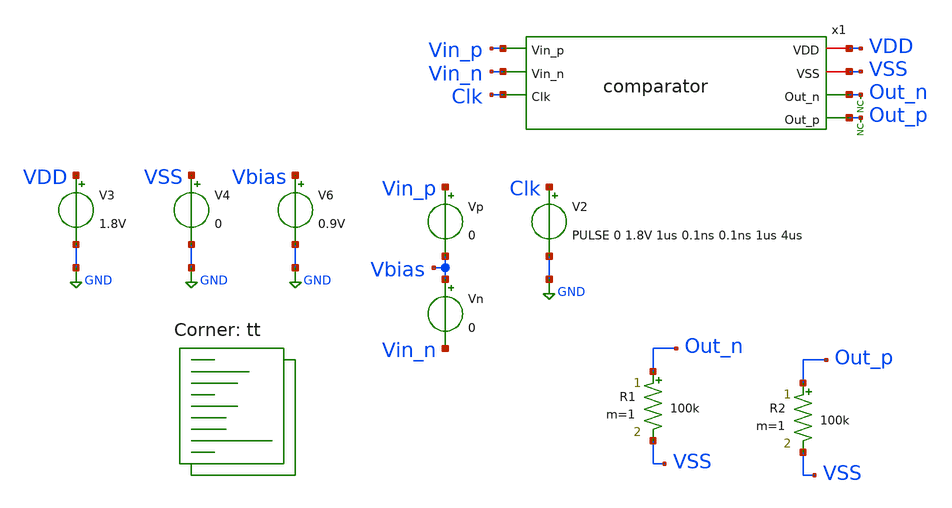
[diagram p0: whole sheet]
** sch_path: xschem/tests/comparator/comparator_stepped_test2.sch
**.subckt comparator_stepped_test2
V3 VDD GND 1.8V
V4 VSS GND 0
x1 VDD VSS Vin_p Out_n Vin_n Out_p Clk comparator
Vp Vin_p Vbias 0
V2 Clk GND PULSE 0 1.8V 1us 0.1ns 0.1ns 1us 4us
* noconn Out_p
* noconn Out_n
Vn Vbias Vin_n 0
V6 Vbias GND 0.9V
R1 Out_n VSS 100k m=1
R2 Out_p VSS 100k m=1
**** begin user architecture code
 *.lib $::SKYWATER_MODELS/sky130.lib.spice tt
.include $::SKYWATER_STDCELLS/sky130_fd_sc_hd.spice

.lib $::SKYWATER_MODELS/sky130.lib.spice tt



* ngspice commands


.control
save all
let vdiff = -0.1V
let vmax = 0.1V
let vdelta = 1.8e-2;
let runs = 0
let bad = 0
set sum_file = comparator_test_issues.txt
let bad_vdiffs = 0
set wr_vecnames

while vdiff le $&vmax
	alter vp vdiff
	alter vn vdiff
	tran 0.01u 3u
	*plot vin_p-vin_n out_p+4 out_n+4
	meas tran p_max MAX v(out_p) from=0u to=3u
	meas tran n_max MAX v(out_n) from=0u to=3u

	if $&vdiff > 0
		if $&p_max > 0.9
			if $&n_max < 0.9
				echo Good: $&vdiff
			else
				*compose bad_vdiffs values $&bad_vdiffs $&vdiff

				set fn = test_comparator_step_{$&vdiff}.txt
				echo Writing $fn
				wrdata $fn out_n out_p

				let bad = bad + 1

				echo Bad: $&vdiff
			end
		else
			*compose bad_vdiffs values $&bad_vdiffs $&vdiff
			set fn = test_comparator_step_{$&vdiff}.txt
			echo Writing $fn
			wrdata $fn out_n out_p

			let bad = bad + 1

			echo Bad: $&vdiff
		end
	else
		if $&p_max < 0.9
			if $&n_max > 0.9
				echo Good: $&vdiff
			else
				compose bad_vdiffs values $&bad_vdiffs $&vdiff

				set fn = test_comparator_step_{$&vdiff}.txt
				echo Writing $fn
				wrdata $fn out_n out_p

				let bad = bad + 1

				echo Bad: $&vdiff
			end
		else
			compose bad_vdiffs values $&bad_vdiffs $&vdiff

			set fn = test_comparator_step_{$&vdiff}.txt
			echo Writing $fn
			wrdata $fn out_n out_p

			let bad = bad + 1

			echo Bad: $&vdiff
		end

	end


	* set fn = test_comparator_step_{$&vdiff}.txt
	* echo Writing $fn
	* wrdata $fn out_n out_p

	echo run $&runs
	let vdiff = vdiff + vdelta
	let runs = runs + 1

	destroy all

end

*wrdata {$sum_file} bad_vdiffs

echo
echo Total Runs = $&runs
echo Total Bad = $&bad
echo
.endc



**** end user architecture code
**.ends

* expanding   symbol:  src/comparator/comparator.sym # of pins=7
** sym_path: xschem/src/comparator/comparator.sym
** sch_path: xschem/src/comparator/comparator.sch
.subckt comparator VDD VSS Vin_p Out_n Vin_n Out_p Clk
*.iopin VDD
*.iopin VSS
*.ipin Vin_p
*.opin Out_n
*.ipin Vin_n
*.opin Out_p
*.ipin Clk
XM1 Pre_Amp_n Clk VDD VSS sky130_fd_pr__pfet_01v8 L=0.15 W=1 nf=1 ad='int((nf+1)/2) * W/nf * 0.29' as='int((nf+2)/2) * W/nf * 0.29'
+ pd='2*int((nf+1)/2) * (W/nf + 0.29)' ps='2*int((nf+2)/2) * (W/nf + 0.29)' nrd='0.29 / W' nrs='0.29 / W'
+ sa=0 sb=0 sd=0 mult=1 m=1
XM2 Pre_Amp_p Clk VDD VSS sky130_fd_pr__pfet_01v8 L=0.15 W=1 nf=1 ad='int((nf+1)/2) * W/nf * 0.29' as='int((nf+2)/2) * W/nf * 0.29'
+ pd='2*int((nf+1)/2) * (W/nf + 0.29)' ps='2*int((nf+2)/2) * (W/nf + 0.29)' nrd='0.29 / W' nrs='0.29 / W'
+ sa=0 sb=0 sd=0 mult=1 m=1
XM3 Pre_Amp_p Vin_p net1 VSS sky130_fd_pr__nfet_01v8 L=0.15 W=1 nf=1 ad='int((nf+1)/2) * W/nf * 0.29'
+ as='int((nf+2)/2) * W/nf * 0.29' pd='2*int((nf+1)/2) * (W/nf + 0.29)' ps='2*int((nf+2)/2) * (W/nf + 0.29)'
+ nrd='0.29 / W' nrs='0.29 / W' sa=0 sb=0 sd=0 mult=1 m=1
XM4 Pre_Amp_n Vin_n net1 VSS sky130_fd_pr__nfet_01v8 L=0.15 W=1 nf=1 ad='int((nf+1)/2) * W/nf * 0.29'
+ as='int((nf+2)/2) * W/nf * 0.29' pd='2*int((nf+1)/2) * (W/nf + 0.29)' ps='2*int((nf+2)/2) * (W/nf + 0.29)'
+ nrd='0.29 / W' nrs='0.29 / W' sa=0 sb=0 sd=0 mult=1 m=1
XM5 net3 Out_p VDD VSS sky130_fd_pr__pfet_01v8 L=0.15 W=1 nf=1 ad='int((nf+1)/2) * W/nf * 0.29' as='int((nf+2)/2) * W/nf * 0.29'
+ pd='2*int((nf+1)/2) * (W/nf + 0.29)' ps='2*int((nf+2)/2) * (W/nf + 0.29)' nrd='0.29 / W' nrs='0.29 / W'
+ sa=0 sb=0 sd=0 mult=1 m=1
XM6 net2 Out_n VDD VSS sky130_fd_pr__pfet_01v8 L=0.15 W=1 nf=1 ad='int((nf+1)/2) * W/nf * 0.29' as='int((nf+2)/2) * W/nf * 0.29'
+ pd='2*int((nf+1)/2) * (W/nf + 0.29)' ps='2*int((nf+2)/2) * (W/nf + 0.29)' nrd='0.29 / W' nrs='0.29 / W'
+ sa=0 sb=0 sd=0 mult=1 m=1
XM7 net2 Pre_Amp_p Out_p VSS sky130_fd_pr__nfet_01v8 L=0.15 W=1 nf=1 ad='int((nf+1)/2) * W/nf * 0.29'
+ as='int((nf+2)/2) * W/nf * 0.29' pd='2*int((nf+1)/2) * (W/nf + 0.29)' ps='2*int((nf+2)/2) * (W/nf + 0.29)'
+ nrd='0.29 / W' nrs='0.29 / W' sa=0 sb=0 sd=0 mult=1 m=1
XM8 net3 Pre_Amp_n Out_n VSS sky130_fd_pr__nfet_01v8 L=0.15 W=1 nf=1 ad='int((nf+1)/2) * W/nf * 0.29'
+ as='int((nf+2)/2) * W/nf * 0.29' pd='2*int((nf+1)/2) * (W/nf + 0.29)' ps='2*int((nf+2)/2) * (W/nf + 0.29)'
+ nrd='0.29 / W' nrs='0.29 / W' sa=0 sb=0 sd=0 mult=1 m=1
XM9 net1 Clk VSS VSS sky130_fd_pr__nfet_01v8 L=0.15 W=1 nf=1 ad='int((nf+1)/2) * W/nf * 0.29' as='int((nf+2)/2) * W/nf * 0.29'
+ pd='2*int((nf+1)/2) * (W/nf + 0.29)' ps='2*int((nf+2)/2) * (W/nf + 0.29)' nrd='0.29 / W' nrs='0.29 / W'
+ sa=0 sb=0 sd=0 mult=1 m=1
XM10 Pre_Amp_n Vin_n net1 VSS sky130_fd_pr__nfet_01v8 L=0.15 W=1 nf=1 ad='int((nf+1)/2) * W/nf * 0.29'
+ as='int((nf+2)/2) * W/nf * 0.29' pd='2*int((nf+1)/2) * (W/nf + 0.29)' ps='2*int((nf+2)/2) * (W/nf + 0.29)'
+ nrd='0.29 / W' nrs='0.29 / W' sa=0 sb=0 sd=0 mult=1 m=1
XM11 Out_n Clk_n VSS VSS sky130_fd_pr__nfet_01v8 L=0.15 W=1 nf=1 ad='int((nf+1)/2) * W/nf * 0.29' as='int((nf+2)/2) * W/nf * 0.29'
+ pd='2*int((nf+1)/2) * (W/nf + 0.29)' ps='2*int((nf+2)/2) * (W/nf + 0.29)' nrd='0.29 / W' nrs='0.29 / W'
+ sa=0 sb=0 sd=0 mult=1 m=1
XM12 Out_n Out_p VSS VSS sky130_fd_pr__nfet_01v8 L=0.15 W=1 nf=1 ad='int((nf+1)/2) * W/nf * 0.29' as='int((nf+2)/2) * W/nf * 0.29'
+ pd='2*int((nf+1)/2) * (W/nf + 0.29)' ps='2*int((nf+2)/2) * (W/nf + 0.29)' nrd='0.29 / W' nrs='0.29 / W'
+ sa=0 sb=0 sd=0 mult=1 m=1
XM13 Out_p Out_n VSS VSS sky130_fd_pr__nfet_01v8 L=0.15 W=1 nf=1 ad='int((nf+1)/2) * W/nf * 0.29' as='int((nf+2)/2) * W/nf * 0.29'
+ pd='2*int((nf+1)/2) * (W/nf + 0.29)' ps='2*int((nf+2)/2) * (W/nf + 0.29)' nrd='0.29 / W' nrs='0.29 / W'
+ sa=0 sb=0 sd=0 mult=1 m=1
XM14 Out_p Clk_n VSS VSS sky130_fd_pr__nfet_01v8 L=0.15 W=1 nf=1 ad='int((nf+1)/2) * W/nf * 0.29' as='int((nf+2)/2) * W/nf * 0.29'
+ pd='2*int((nf+1)/2) * (W/nf + 0.29)' ps='2*int((nf+2)/2) * (W/nf + 0.29)' nrd='0.29 / W' nrs='0.29 / W'
+ sa=0 sb=0 sd=0 mult=1 m=1
XM15 Clk_n Clk VDD VSS sky130_fd_pr__pfet_01v8 L=0.15 W=1 nf=1 ad='int((nf+1)/2) * W/nf * 0.29' as='int((nf+2)/2) * W/nf * 0.29'
+ pd='2*int((nf+1)/2) * (W/nf + 0.29)' ps='2*int((nf+2)/2) * (W/nf + 0.29)' nrd='0.29 / W' nrs='0.29 / W'
+ sa=0 sb=0 sd=0 mult=1 m=1
XM16 Clk_n Clk VSS VSS sky130_fd_pr__nfet_01v8 L=0.15 W=1 nf=1 ad='int((nf+1)/2) * W/nf * 0.29' as='int((nf+2)/2) * W/nf * 0.29'
+ pd='2*int((nf+1)/2) * (W/nf + 0.29)' ps='2*int((nf+2)/2) * (W/nf + 0.29)' nrd='0.29 / W' nrs='0.29 / W'
+ sa=0 sb=0 sd=0 mult=1 m=1
.ends

.GLOBAL GND
.end
